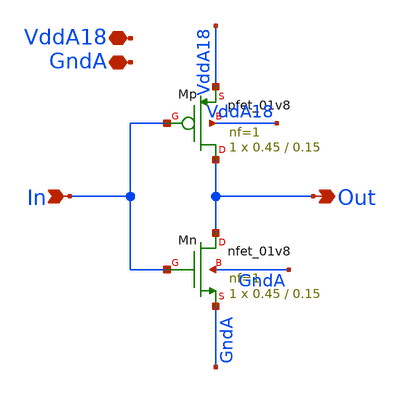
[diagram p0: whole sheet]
** sch_path: analog/klayout/production/final_merge_20260923/testbenches/cace/analog/xschem/Bias_Inv_Decoder.sch
**.subckt Bias_Inv_Decoder In GndA VddA18 Out
*.ipin In
*.iopin GndA
*.iopin VddA18
*.opin Out
XMp Out In VddA18 VddA18 sky130_fd_pr__pfet_01v8 L=0.15 W=0.45 nf=1 ad='int((1 + 1)/2) * 0.45 / 1 * 0.29'
+ as='int((1 + 2)/2) * 0.45 / 1 * 0.29' pd='2*int((1 + 1)/2) * (0.45 / 1 + 0.29)' ps='2*int((1 + 2)/2) * (0.45 / 1 + 0.29)'
+ nrd='0.29 / 0.45 ' nrs='0.29 / 0.45 ' sa=0 sb=0 sd=0 mult=1 m=1
XMn Out In GndA GndA sky130_fd_pr__nfet_01v8 L=0.15 W=0.45 nf=1 ad='int((1 + 1)/2) * 0.45 / 1 * 0.29'
+ as='int((1 + 2)/2) * 0.45 / 1 * 0.29' pd='2*int((1 + 1)/2) * (0.45 / 1 + 0.29)' ps='2*int((1 + 2)/2) * (0.45 / 1 + 0.29)'
+ nrd='0.29 / 0.45 ' nrs='0.29 / 0.45 ' sa=0 sb=0 sd=0 mult=1 m=1
**.ends
.end
